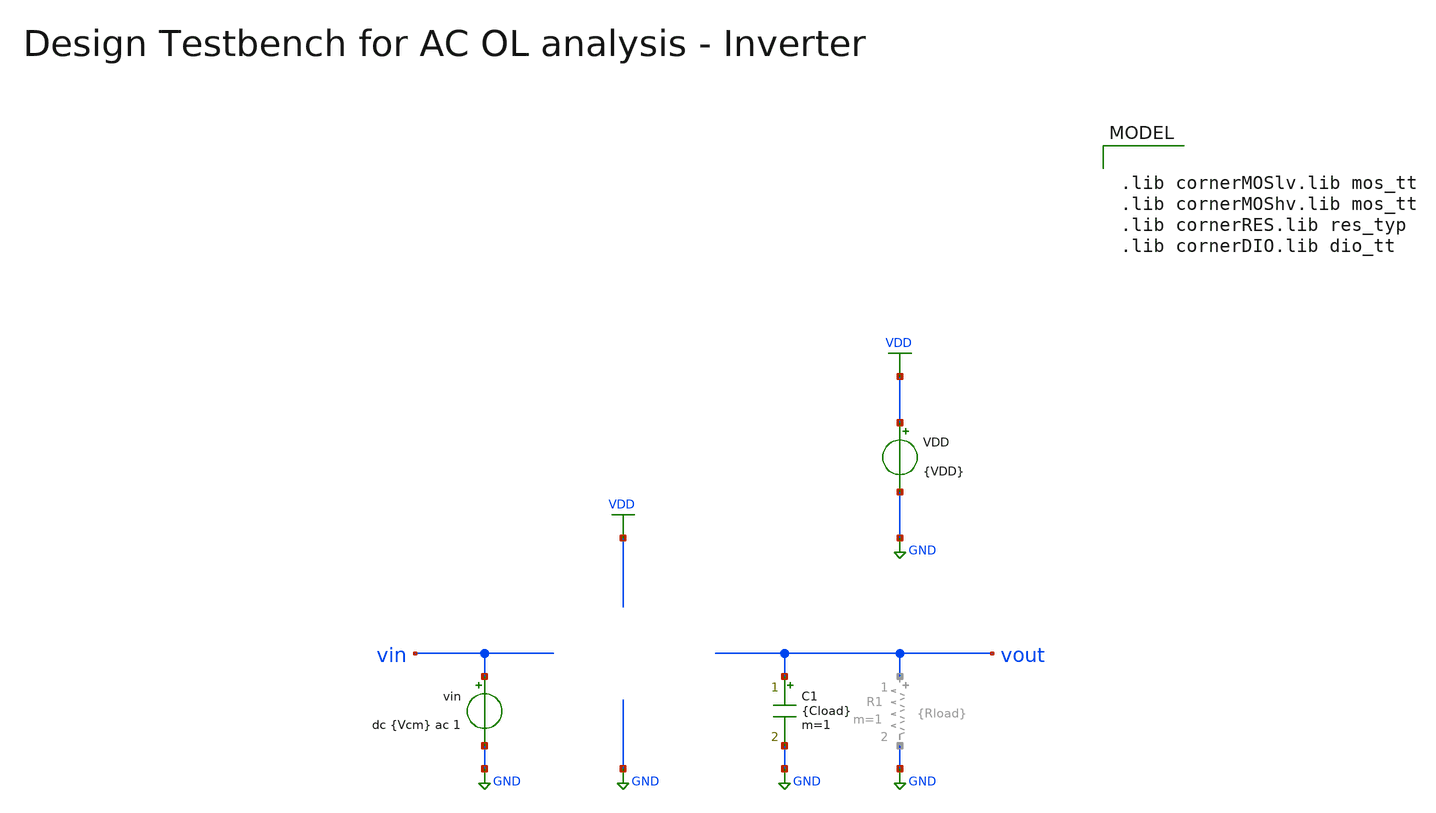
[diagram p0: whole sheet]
** sch_path: inverter/testbenches/xschem/inverter_tb_ac_ol.sch
**.subckt inverter_tb_ac_ol
VDD VDD GND {VDD}
vin vin GND dc {Vcm} ac 1
C1 vout GND {Cload} m=1
**** begin user architecture code


*.include ../../../netlist/pex/inverter_magic_pex_3.spice
.param VDD=1.5
.param Vcm=VDD/2
.param temp=27
.param Cload=10p
.param Rload=1k
.options savecurrents klu method=gear reltol=1e-4 abstol=1e-15 gmin=1e-15
.control

save all

set wr_vecnames
set wr_singlescale

* User Constants
let f_min = 0.1
let f_max = 10G
let fdc = 1

* Operating Point Analysis
op
remzerovec
write @schname\.raw
set appendwrite

* AC Analysis
ac dec 101 $&const.f_min $&const.f_max
remzerovec
write @schname\.raw

* Plotting
let Aol = v(vout)/v(vin)
let Aol_dB = vdb(Aol)
let Aol_arg = 180/PI*cphase(Aol)

plot Aol_dB ylabel 'Magnitude'
plot Aol_arg ylabel 'Phase'
plot Aol_dB Aol_arg ylabel 'Magnitude, Phase'

* Measurements
* DC open-loop gain
meas ac Adc_ol_dB find Aol_dB when frequency = fdc
print Adc_ol_dB

* 3dB cut-off frequency
let Aol_fc = Adc_ol_dB - 3
meas ac fc find frequency when Aol_dB = Aol_fc
print fc

* Unity Gain Bandwidth (Aol=1 or Aol_dB = 0dB)
meas ac UGB when Aol_dB=0  fall=1
print UGB

* Phase Margin at Aol=1 or Aol_dB = 0dB
meas ac arg_0dB find Aol_arg when Aol_dB=0
let PM = 180-abs(arg_0dB)
print PM

* Write Data
unset appendwrite
set wr_vecnames
set wr_singlescale
wrdata ../plot_simulations/data/@schname\.txt v(Aol_dB) v(Aol_arg)

*quit
.endc



.lib cornerMOSlv.lib mos_tt
.lib cornerMOShv.lib mos_tt
.lib cornerRES.lib res_typ
.lib cornerDIO.lib dio_tt

**** end user architecture code
**.ends
.GLOBAL GND
.GLOBAL VDD
.end
